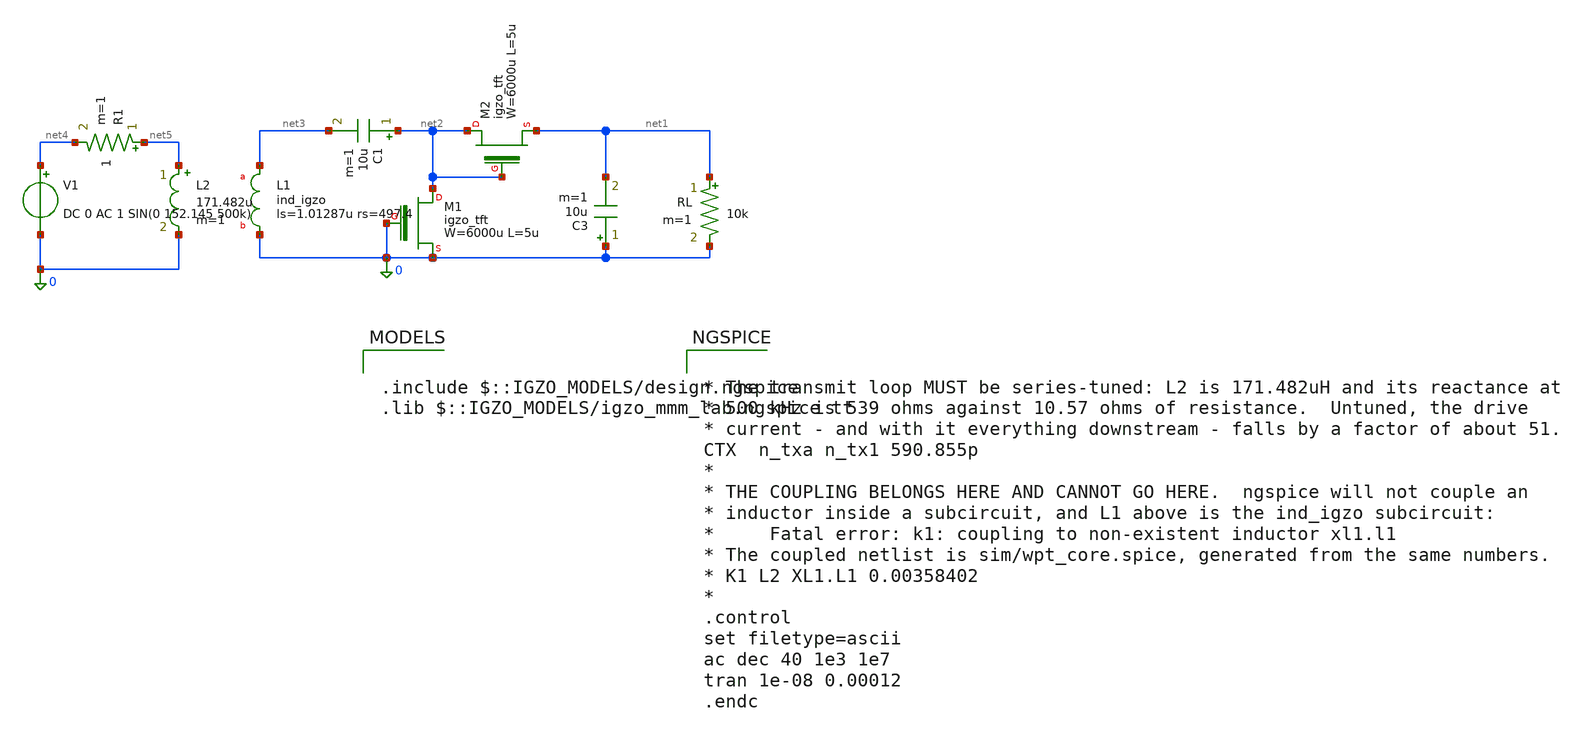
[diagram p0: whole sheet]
** sch_path: WPT/WPT.sch
**.subckt WPT
XL1 net3 0 ind_igzo ls=1.01287u rs=497.4
C1 net2 net3 10u m=1
XM1 net2 0 0 igzo_tft W=6000u L=5u ov=2u nf=1 m=1
XM2 net2 net2 net1 igzo_tft W=6000u L=5u ov=2u nf=1 m=1
C3 0 net1 10u m=1
RL net1 0 10k m=1
V1 net4 0 DC 0 AC 1 SIN(0 152.145 500k)
.save i(v1)
R1 net5 net4 1 m=1
L2 net5 0 171.482u m=1
**** begin user architecture code

.include $::IGZO_MODELS/design.ngspice
.lib $::IGZO_MODELS/igzo_mmm_lab.ngspice tt



* The transmit loop MUST be series-tuned: L2 is 171.482uH and its reactance at
* 500 kHz is 539 ohms against 10.57 ohms of resistance.  Untuned, the drive
* current - and with it everything downstream - falls by a factor of about 51.
CTX  n_txa n_tx1 590.855p
*
* THE COUPLING BELONGS HERE AND CANNOT GO HERE.  ngspice will not couple an
* inductor inside a subcircuit, and L1 above is the ind_igzo subcircuit:
*     Fatal error: k1: coupling to non-existent inductor xl1.l1
* The coupled netlist is sim/wpt_core.spice, generated from the same numbers.
* K1 L2 XL1.L1 0.00358402
*
.control
set filetype=ascii
ac dec 40 1e3 1e7
tran 1e-08 0.00012
.endc


**** end user architecture code
**.ends
.end
